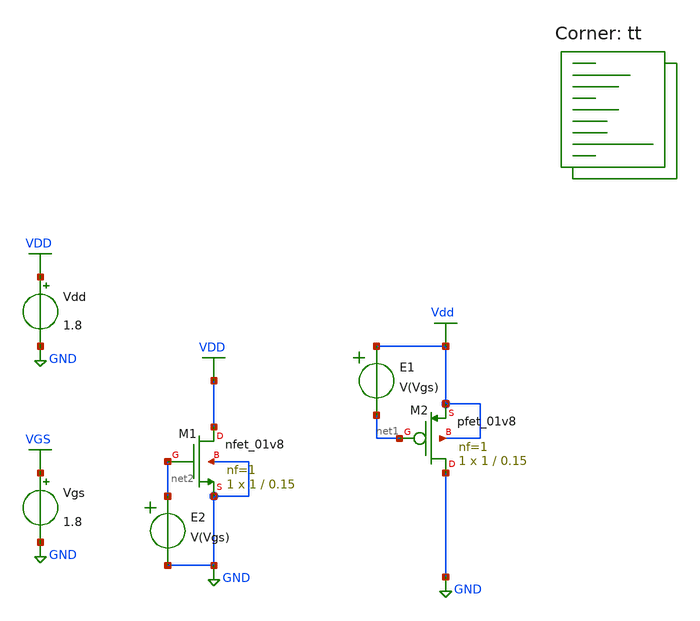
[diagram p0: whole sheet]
** sch_path: characterization.sch
**.subckt characterization
Vgs VGS GND 1.8
Vdd VDD GND 1.8
E1 Vdd net1 VOL=' V(Vgs) '
E2 net2 GND VOL=' V(Vgs) '
XM1 VDD net2 GND GND sky130_fd_pr__nfet_01v8 L=0.15 W=1 nf=1 ad='int((nf+1)/2) * W/nf * 0.29' as='int((nf+2)/2) * W/nf * 0.29'
+ pd='2*int((nf+1)/2) * (W/nf + 0.29)' ps='2*int((nf+2)/2) * (W/nf + 0.29)' nrd='0.29 / W' nrs='0.29 / W'
+ sa=0 sb=0 sd=0 mult=1 m=1
XM2 GND net1 Vdd Vdd sky130_fd_pr__pfet_01v8 L=0.15 W=1 nf=1 ad='int((nf+1)/2) * W/nf * 0.29' as='int((nf+2)/2) * W/nf * 0.29'
+ pd='2*int((nf+1)/2) * (W/nf + 0.29)' ps='2*int((nf+2)/2) * (W/nf + 0.29)' nrd='0.29 / W' nrs='0.29 / W'
+ sa=0 sb=0 sd=0 mult=1 m=1
**** begin user architecture code



.options savecurrents

.control
save all
dc Vgs 0 1.8 0.01

let id_nmos=@m.xm1.msky130_fd_pr__nfet_01v8[id]
let id_pmos=@m.xm2.msky130_fd_pr__pfet_01v8[id]

plot sqrt(id_nmos) sqrt(id_pmos) title 'V_GS characteristic' xlabel 'V_GS' ylabel 'Current'

write characterization.raw
set appendwrite
.endc


.lib $::SKYWATER_MODELS/sky130.lib.spice tt
**** end user architecture code
**.ends
.GLOBAL GND
.GLOBAL VGS
.GLOBAL VDD
.GLOBAL Vdd
.end
